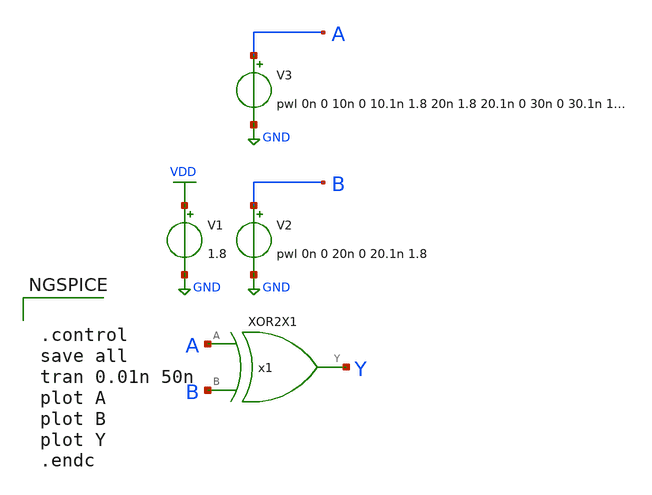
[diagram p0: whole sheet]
** sch_path: layout/xschem/sky130_rhbd/testbenches/test_XOR2X1.sch
**.subckt test_XOR2X1
V2 B GND pwl 0n 0 20n 0 20.1n 1.8
V1 VDD GND 1.8
V3 A GND pwl 0n 0 10n 0 10.1n 1.8 20n 1.8 20.1n 0 30n 0 30.1n 1.8 40n 1.8 40.1n 0
x1 Y A B VDD GND XOR2X1
**** begin user architecture code

.lib $::SKYWATER_MODELS/sky130.lib.spice tt


**** end user architecture code
**.ends
.GLOBAL VDD
.GLOBAL GND
**** begin user architecture code


.control
save all
tran 0.01n 50n
plot A
plot B
plot Y
.endc


**** end user architecture code
.end
